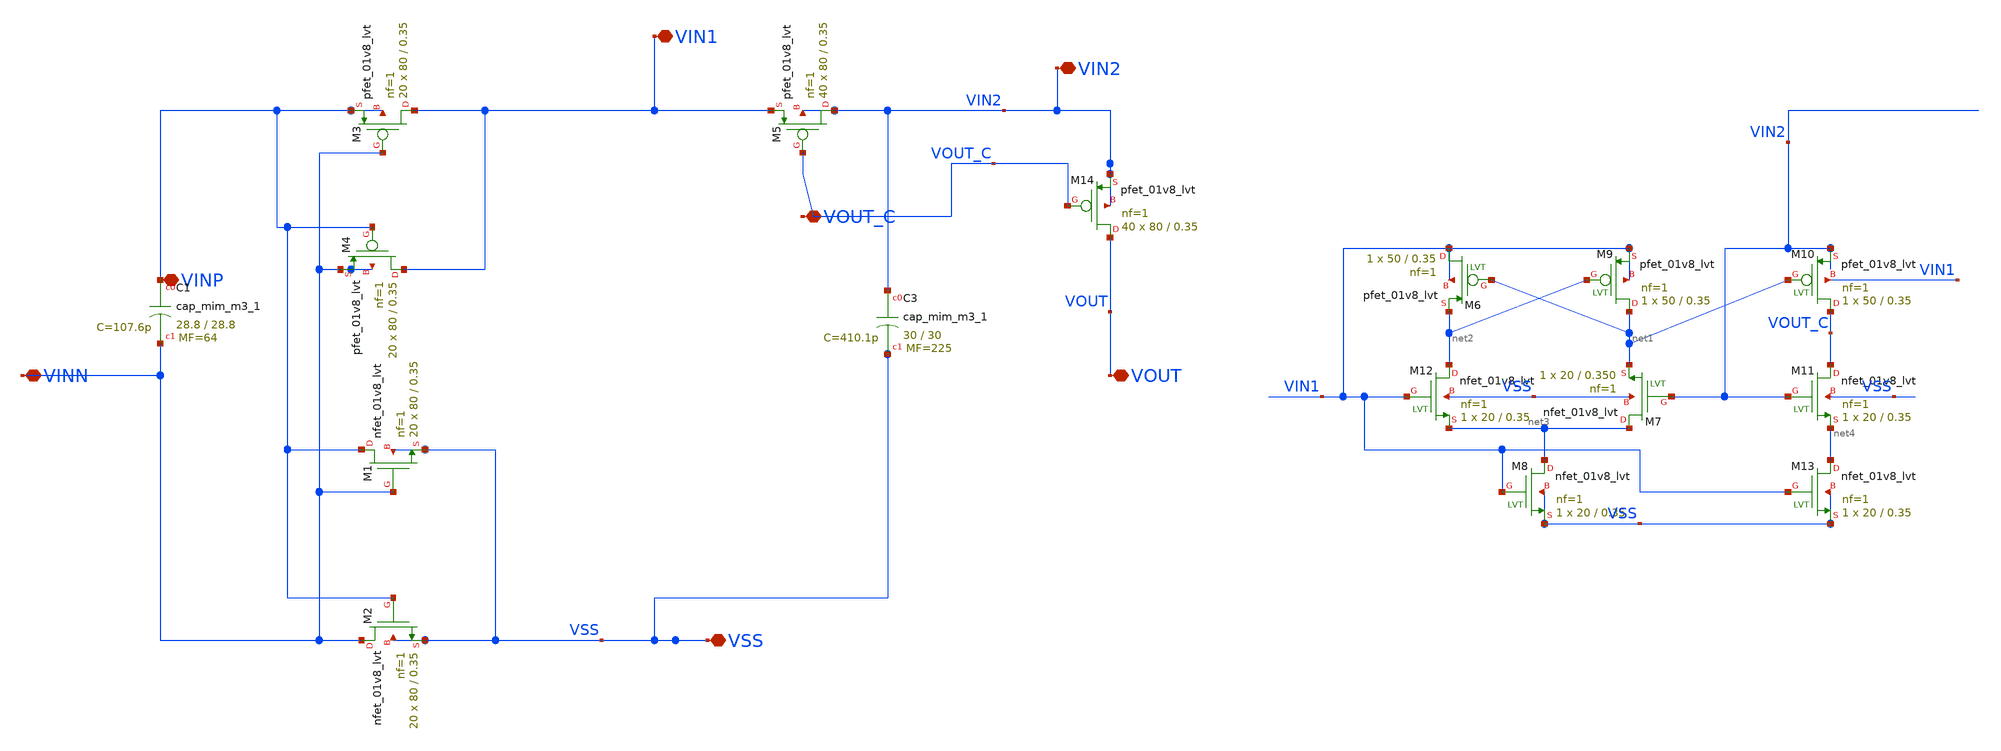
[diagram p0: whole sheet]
** sch_path: LVS/FINAL_SCHEMATIC.sch
**.subckt FINAL_SCHEMATIC VIN1 VINN VSS VINP VOUT_C VOUT VIN2
*.iopin VIN1
*.iopin VINN
*.iopin VSS
*.iopin VINP
*.iopin VOUT_C
*.iopin VOUT
*.iopin VIN2
XM1 VINP VINN VSS VSS sky130_fd_pr__nfet_01v8_lvt L=0.35 W=80 nf=1 ad='int((nf+1)/2) * W/nf * 0.29' as='int((nf+2)/2) * W/nf * 0.29'
+ pd='2*int((nf+1)/2) * (W/nf + 0.29)' ps='2*int((nf+2)/2) * (W/nf + 0.29)' nrd='0.29 / W' nrs='0.29 / W'
+ sa=0 sb=0 sd=0 mult=20 m=20
XM2 VINN VINP VSS VSS sky130_fd_pr__nfet_01v8_lvt L=0.35 W=80 nf=1 ad='int((nf+1)/2) * W/nf * 0.29' as='int((nf+2)/2) * W/nf * 0.29'
+ pd='2*int((nf+1)/2) * (W/nf + 0.29)' ps='2*int((nf+2)/2) * (W/nf + 0.29)' nrd='0.29 / W' nrs='0.29 / W'
+ sa=0 sb=0 sd=0 mult=20 m=20
XM4 VIN1 VINP VINN VINN sky130_fd_pr__pfet_01v8_lvt L=0.35 W=80 nf=1 ad='int((nf+1)/2) * W/nf * 0.29'
+ as='int((nf+2)/2) * W/nf * 0.29' pd='2*int((nf+1)/2) * (W/nf + 0.29)' ps='2*int((nf+2)/2) * (W/nf + 0.29)'
+ nrd='0.29 / W' nrs='0.29 / W' sa=0 sb=0 sd=0 mult=20 m=20
XM3 VIN1 VINN VINP VINP sky130_fd_pr__pfet_01v8_lvt L=0.35 W=80 nf=1 ad='int((nf+1)/2) * W/nf * 0.29'
+ as='int((nf+2)/2) * W/nf * 0.29' pd='2*int((nf+1)/2) * (W/nf + 0.29)' ps='2*int((nf+2)/2) * (W/nf + 0.29)'
+ nrd='0.29 / W' nrs='0.29 / W' sa=0 sb=0 sd=0 mult=20 m=20
XM5 VIN2 VOUT_C VIN1 VIN2 sky130_fd_pr__pfet_01v8_lvt L=0.35 W=80 nf=1 ad='int((nf+1)/2) * W/nf * 0.29'
+ as='int((nf+2)/2) * W/nf * 0.29' pd='2*int((nf+1)/2) * (W/nf + 0.29)' ps='2*int((nf+2)/2) * (W/nf + 0.29)'
+ nrd='0.29 / W' nrs='0.29 / W' sa=0 sb=0 sd=0 mult=40 m=40
XM14 VOUT VOUT_C VIN2 VIN2 sky130_fd_pr__pfet_01v8_lvt L=0.35 W=80 nf=1 ad='int((nf+1)/2) * W/nf * 0.29'
+ as='int((nf+2)/2) * W/nf * 0.29' pd='2*int((nf+1)/2) * (W/nf + 0.29)' ps='2*int((nf+2)/2) * (W/nf + 0.29)'
+ nrd='0.29 / W' nrs='0.29 / W' sa=0 sb=0 sd=0 mult=40 m=40
XC3 VIN2 VSS sky130_fd_pr__cap_mim_m3_1 W=30 L=30 MF=225 m=225
XM6 VIN1 net1 net2 VIN1 sky130_fd_pr__pfet_01v8_lvt L=0.35 W=50 nf=1 ad='int((nf+1)/2) * W/nf * 0.29'
+ as='int((nf+2)/2) * W/nf * 0.29' pd='2*int((nf+1)/2) * (W/nf + 0.29)' ps='2*int((nf+2)/2) * (W/nf + 0.29)'
+ nrd='0.29 / W' nrs='0.29 / W' sa=0 sb=0 sd=0 mult=1 m=1
XM7 net3 VIN2 net1 VSS sky130_fd_pr__nfet_01v8_lvt L=0.350 W=20 nf=1 ad='int((nf+1)/2) * W/nf * 0.29'
+ as='int((nf+2)/2) * W/nf * 0.29' pd='2*int((nf+1)/2) * (W/nf + 0.29)' ps='2*int((nf+2)/2) * (W/nf + 0.29)'
+ nrd='0.29 / W' nrs='0.29 / W' sa=0 sb=0 sd=0 mult=1 m=1
XM8 net3 VIN1 VSS VSS sky130_fd_pr__nfet_01v8_lvt L=0.35 W=20 nf=1 ad='int((nf+1)/2) * W/nf * 0.29' as='int((nf+2)/2) * W/nf * 0.29'
+ pd='2*int((nf+1)/2) * (W/nf + 0.29)' ps='2*int((nf+2)/2) * (W/nf + 0.29)' nrd='0.29 / W' nrs='0.29 / W'
+ sa=0 sb=0 sd=0 mult=1 m=1
XM9 net1 net2 VIN1 VIN1 sky130_fd_pr__pfet_01v8_lvt L=0.35 W=50 nf=1 ad='int((nf+1)/2) * W/nf * 0.29'
+ as='int((nf+2)/2) * W/nf * 0.29' pd='2*int((nf+1)/2) * (W/nf + 0.29)' ps='2*int((nf+2)/2) * (W/nf + 0.29)'
+ nrd='0.29 / W' nrs='0.29 / W' sa=0 sb=0 sd=0 mult=1 m=1
XM10 VOUT_C net1 VIN2 VIN1 sky130_fd_pr__pfet_01v8_lvt L=0.35 W=50 nf=1 ad='int((nf+1)/2) * W/nf * 0.29'
+ as='int((nf+2)/2) * W/nf * 0.29' pd='2*int((nf+1)/2) * (W/nf + 0.29)' ps='2*int((nf+2)/2) * (W/nf + 0.29)'
+ nrd='0.29 / W' nrs='0.29 / W' sa=0 sb=0 sd=0 mult=1 m=1
XM11 VOUT_C VIN2 net4 VSS sky130_fd_pr__nfet_01v8_lvt L=0.35 W=20 nf=1 ad='int((nf+1)/2) * W/nf * 0.29'
+ as='int((nf+2)/2) * W/nf * 0.29' pd='2*int((nf+1)/2) * (W/nf + 0.29)' ps='2*int((nf+2)/2) * (W/nf + 0.29)'
+ nrd='0.29 / W' nrs='0.29 / W' sa=0 sb=0 sd=0 mult=1 m=1
XM12 net2 VIN1 net3 VSS sky130_fd_pr__nfet_01v8_lvt L=0.35 W=20 nf=1 ad='int((nf+1)/2) * W/nf * 0.29'
+ as='int((nf+2)/2) * W/nf * 0.29' pd='2*int((nf+1)/2) * (W/nf + 0.29)' ps='2*int((nf+2)/2) * (W/nf + 0.29)'
+ nrd='0.29 / W' nrs='0.29 / W' sa=0 sb=0 sd=0 mult=1 m=1
XM13 net4 VIN1 VSS VSS sky130_fd_pr__nfet_01v8_lvt L=0.35 W=20 nf=1 ad='int((nf+1)/2) * W/nf * 0.29'
+ as='int((nf+2)/2) * W/nf * 0.29' pd='2*int((nf+1)/2) * (W/nf + 0.29)' ps='2*int((nf+2)/2) * (W/nf + 0.29)'
+ nrd='0.29 / W' nrs='0.29 / W' sa=0 sb=0 sd=0 mult=1 m=1
XC1 VINP VINN sky130_fd_pr__cap_mim_m3_1 W=28.8 L=28.8 MF=64 m=64
**** begin user architecture code


	.control
	save all
	tran 1ns 10us
	plot v(VOUT)

.endc


 ** manual skywater pdks install (with patches applied)
* .lib $::SKYWATER_MODELS/models/sky130.lib.spice tt

** opencircuitdesign pdks install
.lib $::SKYWATER_MODELS/sky130.lib.spice tt

.param mc_mm_switch=0
.param mc_pr_switch=0

**** end user architecture code
**.ends
.end
